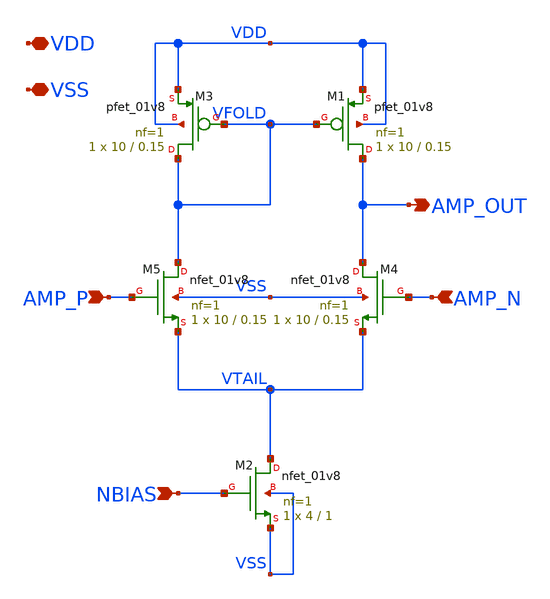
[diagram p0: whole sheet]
** sch_path: xschem/amp.sch
**.subckt amp AMP_P AMP_N AMP_OUT NBIAS VDD VSS
*.ipin AMP_P
*.ipin AMP_N
*.opin AMP_OUT
*.ipin NBIAS
*.iopin VDD
*.iopin VSS
XM3 VFOLD VFOLD VDD VDD sky130_fd_pr__pfet_01v8 L=0.15 W=10 nf=1 ad='int((nf+1)/2) * W/nf * 0.29' as='int((nf+2)/2) * W/nf * 0.29'
+ pd='2*int((nf+1)/2) * (W/nf + 0.29)' ps='2*int((nf+2)/2) * (W/nf + 0.29)' nrd='0.29 / W' nrs='0.29 / W'
+ sa=0 sb=0 sd=0 mult=1 m=1
XM4 AMP_OUT AMP_N VTAIL VSS sky130_fd_pr__nfet_01v8 L=0.15 W=10 nf=1 ad='int((nf+1)/2) * W/nf * 0.29'
+ as='int((nf+2)/2) * W/nf * 0.29' pd='2*int((nf+1)/2) * (W/nf + 0.29)' ps='2*int((nf+2)/2) * (W/nf + 0.29)'
+ nrd='0.29 / W' nrs='0.29 / W' sa=0 sb=0 sd=0 mult=1 m=1
XM1 AMP_OUT VFOLD VDD VDD sky130_fd_pr__pfet_01v8 L=0.15 W=10 nf=1 ad='int((nf+1)/2) * W/nf * 0.29' as='int((nf+2)/2) * W/nf * 0.29'
+ pd='2*int((nf+1)/2) * (W/nf + 0.29)' ps='2*int((nf+2)/2) * (W/nf + 0.29)' nrd='0.29 / W' nrs='0.29 / W'
+ sa=0 sb=0 sd=0 mult=1 m=1
XM5 VFOLD AMP_P VTAIL VSS sky130_fd_pr__nfet_01v8 L=0.15 W=10 nf=1 ad='int((nf+1)/2) * W/nf * 0.29' as='int((nf+2)/2) * W/nf * 0.29'
+ pd='2*int((nf+1)/2) * (W/nf + 0.29)' ps='2*int((nf+2)/2) * (W/nf + 0.29)' nrd='0.29 / W' nrs='0.29 / W'
+ sa=0 sb=0 sd=0 mult=1 m=1
XM2 VTAIL NBIAS VSS VSS sky130_fd_pr__nfet_01v8 L=1 W=4 nf=1 ad='int((nf+1)/2) * W/nf * 0.29' as='int((nf+2)/2) * W/nf * 0.29'
+ pd='2*int((nf+1)/2) * (W/nf + 0.29)' ps='2*int((nf+2)/2) * (W/nf + 0.29)' nrd='0.29 / W' nrs='0.29 / W'
+ sa=0 sb=0 sd=0 mult=1 m=1
**.ends
.end
